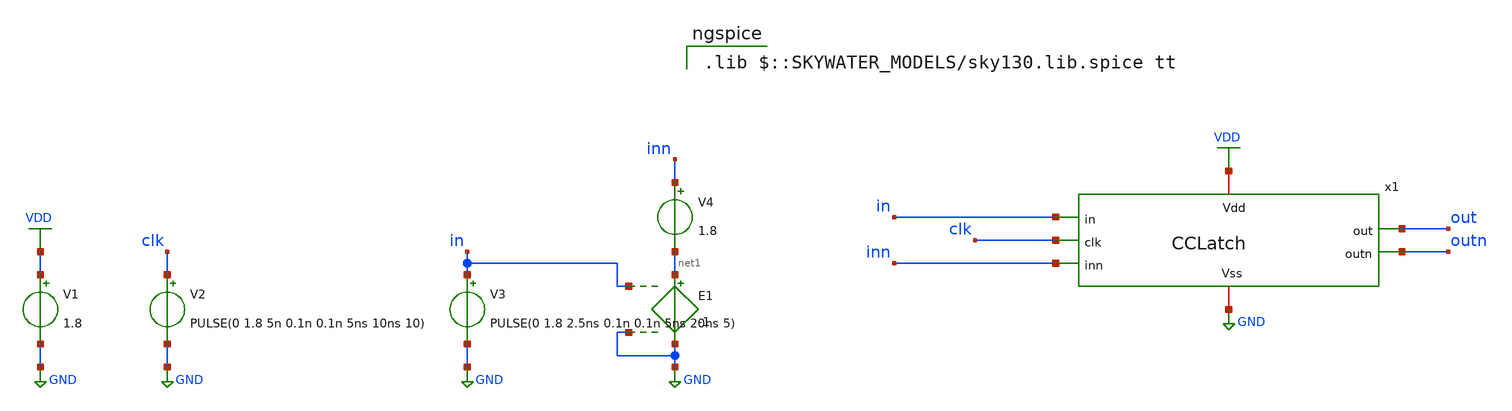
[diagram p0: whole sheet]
** sch_path: Circuits/Examples/Latch/CCLatch_tb.sch
**.subckt CCLatch_tb
x1 VDD out outn in inn clk GND CCLatch
V1 VDD GND 1.8
V2 clk GND PULSE(0 1.8 5n 0.1n 0.1n 5ns 10ns 10)
V3 in GND PULSE(0 1.8 2.5ns 0.1n 0.1n 5ns 20ns 5)
E1 net1 GND in GND -1
V4 inn net1 1.8
**** begin user architecture code



* ngspice commands
.option savecurrents
.save all
.control
tran 1ns 100ns
.endc



 .lib $::SKYWATER_MODELS/sky130.lib.spice tt

**** end user architecture code
**.ends

* expanding   symbol:  /home/jakob/Documents/RALF/Circuits/Examples/Latch/CCLatch.sym # of pins=7
** sym_path: Circuits/Examples/Latch/CCLatch.sym
** sch_path: Circuits/Examples/Latch/CCLatch.sch
.subckt CCLatch Vdd out outn in inn clk Vss
*.iopin Vdd
*.iopin Vss
*.ipin in
*.ipin inn
*.ipin clk
*.opin outn
*.opin out
XM1 outn in Vmid Vss sky130_fd_pr__nfet_01v8 L=1 W=3 nf=1 ad='int((nf+1)/2) * W/nf * 0.29' as='int((nf+2)/2) * W/nf * 0.29'
+ pd='2*int((nf+1)/2) * (W/nf + 0.29)' ps='2*int((nf+2)/2) * (W/nf + 0.29)' nrd='0.29 / W' nrs='0.29 / W'
+ sa=0 sb=0 sd=0 mult=1 m=1
XM2 out inn Vmid Vss sky130_fd_pr__nfet_01v8 L=1 W=3 nf=1 ad='int((nf+1)/2) * W/nf * 0.29' as='int((nf+2)/2) * W/nf * 0.29'
+ pd='2*int((nf+1)/2) * (W/nf + 0.29)' ps='2*int((nf+2)/2) * (W/nf + 0.29)' nrd='0.29 / W' nrs='0.29 / W'
+ sa=0 sb=0 sd=0 mult=1 m=1
XM3 outn out Vdd Vdd sky130_fd_pr__pfet_01v8 L=1 W=1 nf=1 ad='int((nf+1)/2) * W/nf * 0.29' as='int((nf+2)/2) * W/nf * 0.29'
+ pd='2*int((nf+1)/2) * (W/nf + 0.29)' ps='2*int((nf+2)/2) * (W/nf + 0.29)' nrd='0.29 / W' nrs='0.29 / W'
+ sa=0 sb=0 sd=0 mult=1 m=1
XM4 out outn Vdd Vdd sky130_fd_pr__pfet_01v8 L=1 W=1 nf=1 ad='int((nf+1)/2) * W/nf * 0.29' as='int((nf+2)/2) * W/nf * 0.29'
+ pd='2*int((nf+1)/2) * (W/nf + 0.29)' ps='2*int((nf+2)/2) * (W/nf + 0.29)' nrd='0.29 / W' nrs='0.29 / W'
+ sa=0 sb=0 sd=0 mult=1 m=1
XM5 Vmid clk Vss Vss sky130_fd_pr__nfet_01v8 L=1 W=6 nf=2 ad='int((nf+1)/2) * W/nf * 0.29' as='int((nf+2)/2) * W/nf * 0.29'
+ pd='2*int((nf+1)/2) * (W/nf + 0.29)' ps='2*int((nf+2)/2) * (W/nf + 0.29)' nrd='0.29 / W' nrs='0.29 / W'
+ sa=0 sb=0 sd=0 mult=1 m=1
.ends

.GLOBAL VDD
.GLOBAL GND
.end
